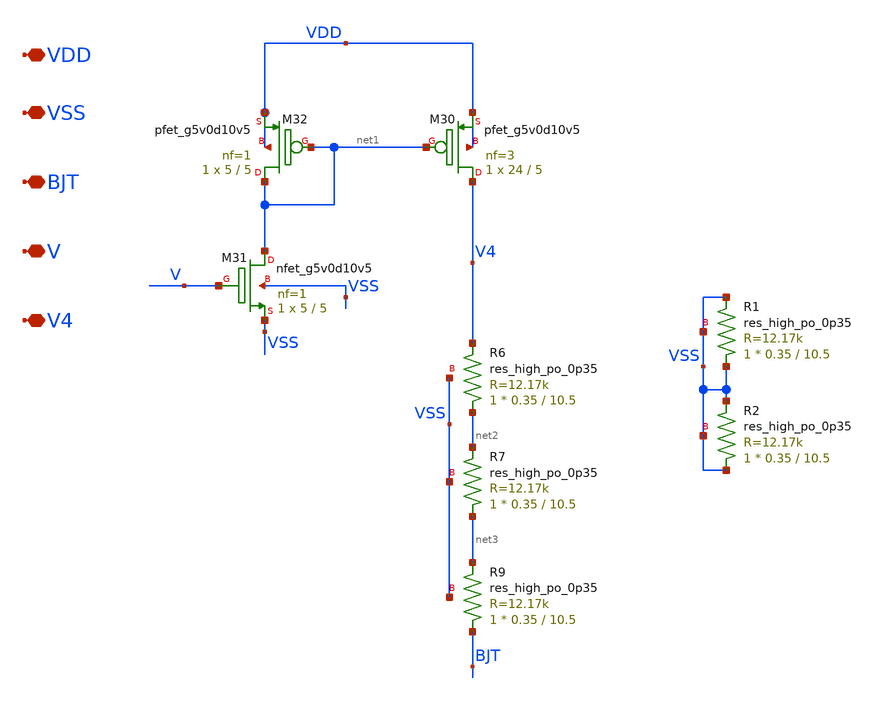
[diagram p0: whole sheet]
** sch_path: xschem/xschem_BGR_Top/BGR_2nd_parta_noBJT_SCH.sch
**.subckt BGR_2nd_parta_noBJT_SCH VSS BJT V V4 VDD
*.iopin VSS
*.iopin BJT
*.iopin V
*.iopin V4
*.iopin VDD
XM30 V4 net1 VDD VDD sky130_fd_pr__pfet_g5v0d10v5 L=5 W=24 nf=3 ad='int((nf+1)/2) * W/nf * 0.29' as='int((nf+2)/2) * W/nf * 0.29'
+ pd='2*int((nf+1)/2) * (W/nf + 0.29)' ps='2*int((nf+2)/2) * (W/nf + 0.29)' nrd='0.29 / W' nrs='0.29 / W'
+ sa=0 sb=0 sd=0 mult=1 m=1
XM31 net1 V VSS VSS sky130_fd_pr__nfet_g5v0d10v5 L=5 W=5 nf=1 ad='int((nf+1)/2) * W/nf * 0.29' as='int((nf+2)/2) * W/nf * 0.29'
+ pd='2*int((nf+1)/2) * (W/nf + 0.29)' ps='2*int((nf+2)/2) * (W/nf + 0.29)' nrd='0.29 / W' nrs='0.29 / W'
+ sa=0 sb=0 sd=0 mult=1 m=1
XM32 net1 net1 VDD VDD sky130_fd_pr__pfet_g5v0d10v5 L=5 W=5 nf=1 ad='int((nf+1)/2) * W/nf * 0.29' as='int((nf+2)/2) * W/nf * 0.29'
+ pd='2*int((nf+1)/2) * (W/nf + 0.29)' ps='2*int((nf+2)/2) * (W/nf + 0.29)' nrd='0.29 / W' nrs='0.29 / W'
+ sa=0 sb=0 sd=0 mult=1 m=1
XR6 net2 V4 VSS sky130_fd_pr__res_high_po_0p35 L=10.5 mult=1 m=1
XR7 net3 net2 VSS sky130_fd_pr__res_high_po_0p35 L=10.5 mult=1 m=1
XR9 BJT net3 VSS sky130_fd_pr__res_high_po_0p35 L=10.5 mult=1 m=1
XR1 VSS VSS VSS sky130_fd_pr__res_high_po_0p35 L=10.5 mult=1 m=1
XR2 VSS VSS VSS sky130_fd_pr__res_high_po_0p35 L=10.5 mult=1 m=1
**.ends
.end
